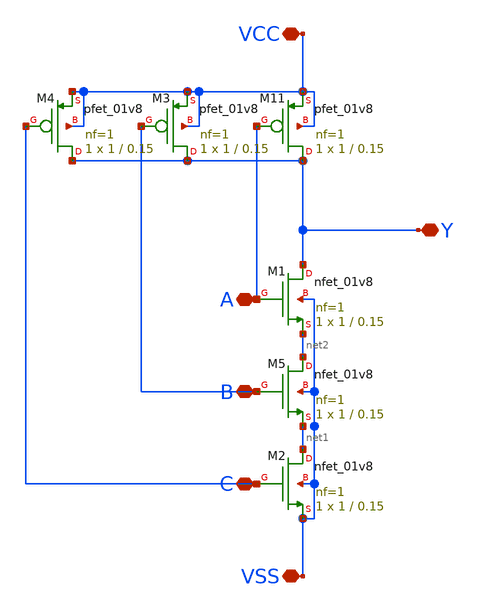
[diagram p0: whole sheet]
** sch_path: logic gates/nand3.sch
**.subckt nand3 VCC VSS Y A B C
*.iopin VCC
*.iopin VSS
*.iopin Y
*.iopin A
*.iopin B
*.iopin C
XM2 net1 C VSS VSS sky130_fd_pr__nfet_01v8 L=0.15 W=1 nf=1 ad='int((1 + 1)/2) * 1 / 1 * 0.29' as='int((1 + 2)/2) * 1 / 1 * 0.29'
+ pd='2*int((1 + 1)/2) * (1 / 1 + 0.29)' ps='2*int((1 + 2)/2) * (1 / 1 + 0.29)' nrd='0.29 / 1 ' nrs='0.29 / 1 '
+ sa=0 sb=0 sd=0 mult=1 m=1
XM11 Y A VCC VCC sky130_fd_pr__pfet_01v8 L=0.15 W=1 nf=1 ad='int((nf+1)/2) * W/nf * 0.29' as='int((nf+2)/2) * W/nf * 0.29'
+ pd='2*int((nf+1)/2) * (W/nf + 0.29)' ps='2*int((nf+2)/2) * (W/nf + 0.29)' nrd='0.29 / W' nrs='0.29 / W'
+ sa=0 sb=0 sd=0 mult=1 m=1
XM1 Y A net2 VSS sky130_fd_pr__nfet_01v8 L=0.15 W=1 nf=1 ad='int((1 + 1)/2) * 1 / 1 * 0.29' as='int((1 + 2)/2) * 1 / 1 * 0.29'
+ pd='2*int((1 + 1)/2) * (1 / 1 + 0.29)' ps='2*int((1 + 2)/2) * (1 / 1 + 0.29)' nrd='0.29 / 1 ' nrs='0.29 / 1 '
+ sa=0 sb=0 sd=0 mult=1 m=1
XM3 Y B VCC VCC sky130_fd_pr__pfet_01v8 L=0.15 W=1 nf=1 ad='int((nf+1)/2) * W/nf * 0.29' as='int((nf+2)/2) * W/nf * 0.29'
+ pd='2*int((nf+1)/2) * (W/nf + 0.29)' ps='2*int((nf+2)/2) * (W/nf + 0.29)' nrd='0.29 / W' nrs='0.29 / W'
+ sa=0 sb=0 sd=0 mult=1 m=1
XM4 Y C VCC VCC sky130_fd_pr__pfet_01v8 L=0.15 W=1 nf=1 ad='int((nf+1)/2) * W/nf * 0.29' as='int((nf+2)/2) * W/nf * 0.29'
+ pd='2*int((nf+1)/2) * (W/nf + 0.29)' ps='2*int((nf+2)/2) * (W/nf + 0.29)' nrd='0.29 / W' nrs='0.29 / W'
+ sa=0 sb=0 sd=0 mult=1 m=1
XM5 net2 B net1 VSS sky130_fd_pr__nfet_01v8 L=0.15 W=1 nf=1 ad='int((1 + 1)/2) * 1 / 1 * 0.29' as='int((1 + 2)/2) * 1 / 1 * 0.29'
+ pd='2*int((1 + 1)/2) * (1 / 1 + 0.29)' ps='2*int((1 + 2)/2) * (1 / 1 + 0.29)' nrd='0.29 / 1 ' nrs='0.29 / 1 '
+ sa=0 sb=0 sd=0 mult=1 m=1
**.ends
.end
